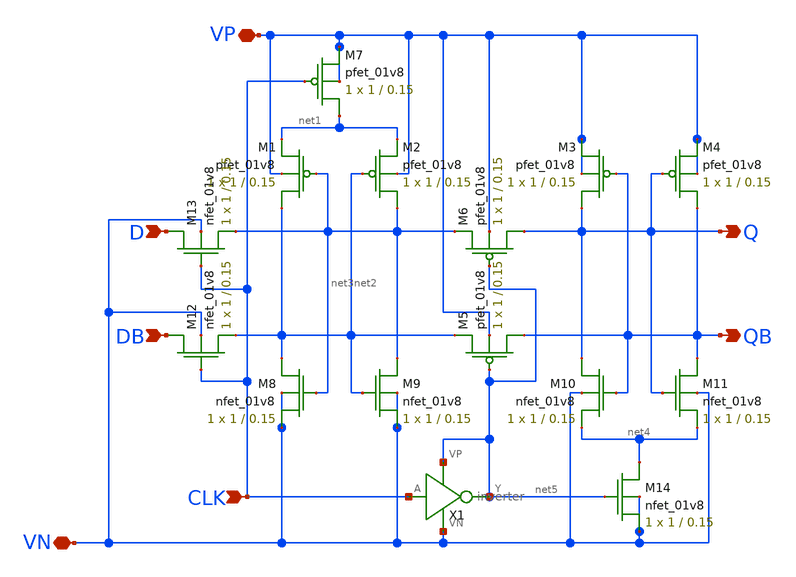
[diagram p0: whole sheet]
** sch_path: MP2/xschem/csrl_dff.sch
**.subckt csrl_dff D DB VP VN CLK QB Q
*.ipin D
*.ipin DB
*.iopin VP
*.iopin VN
*.ipin CLK
*.opin QB
*.opin Q
XM1 net2 net3 net1 VP sky130_fd_pr__pfet_01v8 L=0.15 W=1 nf=1 ad='int((nf+1)/2) * W/nf * 0.29' as='int((nf+2)/2) * W/nf * 0.29'
+ pd='2*int((nf+1)/2) * (W/nf + 0.29)' ps='2*int((nf+2)/2) * (W/nf + 0.29)' nrd='0.29 / W' nrs='0.29 / W'
+ sa=0 sb=0 sd=0 mult=1 m=1
XM2 net3 net2 net1 VP sky130_fd_pr__pfet_01v8 L=0.15 W=1 nf=1 ad='int((nf+1)/2) * W/nf * 0.29' as='int((nf+2)/2) * W/nf * 0.29'
+ pd='2*int((nf+1)/2) * (W/nf + 0.29)' ps='2*int((nf+2)/2) * (W/nf + 0.29)' nrd='0.29 / W' nrs='0.29 / W'
+ sa=0 sb=0 sd=0 mult=1 m=1
XM3 Q QB VP VP sky130_fd_pr__pfet_01v8 L=0.15 W=1 nf=1 ad='int((nf+1)/2) * W/nf * 0.29' as='int((nf+2)/2) * W/nf * 0.29'
+ pd='2*int((nf+1)/2) * (W/nf + 0.29)' ps='2*int((nf+2)/2) * (W/nf + 0.29)' nrd='0.29 / W' nrs='0.29 / W'
+ sa=0 sb=0 sd=0 mult=1 m=1
XM4 QB Q VP VP sky130_fd_pr__pfet_01v8 L=0.15 W=1 nf=1 ad='int((nf+1)/2) * W/nf * 0.29' as='int((nf+2)/2) * W/nf * 0.29'
+ pd='2*int((nf+1)/2) * (W/nf + 0.29)' ps='2*int((nf+2)/2) * (W/nf + 0.29)' nrd='0.29 / W' nrs='0.29 / W'
+ sa=0 sb=0 sd=0 mult=1 m=1
XM8 net2 net3 VN VN sky130_fd_pr__nfet_01v8 L=0.15 W=1 nf=1 ad='int((nf+1)/2) * W/nf * 0.29' as='int((nf+2)/2) * W/nf * 0.29'
+ pd='2*int((nf+1)/2) * (W/nf + 0.29)' ps='2*int((nf+2)/2) * (W/nf + 0.29)' nrd='0.29 / W' nrs='0.29 / W'
+ sa=0 sb=0 sd=0 mult=1 m=1
XM7 net1 CLK VP VP sky130_fd_pr__pfet_01v8 L=0.15 W=1 nf=1 ad='int((nf+1)/2) * W/nf * 0.29' as='int((nf+2)/2) * W/nf * 0.29'
+ pd='2*int((nf+1)/2) * (W/nf + 0.29)' ps='2*int((nf+2)/2) * (W/nf + 0.29)' nrd='0.29 / W' nrs='0.29 / W'
+ sa=0 sb=0 sd=0 mult=1 m=1
XM9 net3 net2 VN VN sky130_fd_pr__nfet_01v8 L=0.15 W=1 nf=1 ad='int((nf+1)/2) * W/nf * 0.29' as='int((nf+2)/2) * W/nf * 0.29'
+ pd='2*int((nf+1)/2) * (W/nf + 0.29)' ps='2*int((nf+2)/2) * (W/nf + 0.29)' nrd='0.29 / W' nrs='0.29 / W'
+ sa=0 sb=0 sd=0 mult=1 m=1
XM10 Q QB net4 VN sky130_fd_pr__nfet_01v8 L=0.15 W=1 nf=1 ad='int((nf+1)/2) * W/nf * 0.29' as='int((nf+2)/2) * W/nf * 0.29'
+ pd='2*int((nf+1)/2) * (W/nf + 0.29)' ps='2*int((nf+2)/2) * (W/nf + 0.29)' nrd='0.29 / W' nrs='0.29 / W'
+ sa=0 sb=0 sd=0 mult=1 m=1
XM11 QB Q net4 VN sky130_fd_pr__nfet_01v8 L=0.15 W=1 nf=1 ad='int((nf+1)/2) * W/nf * 0.29' as='int((nf+2)/2) * W/nf * 0.29'
+ pd='2*int((nf+1)/2) * (W/nf + 0.29)' ps='2*int((nf+2)/2) * (W/nf + 0.29)' nrd='0.29 / W' nrs='0.29 / W'
+ sa=0 sb=0 sd=0 mult=1 m=1
XM12 DB CLK net2 VN sky130_fd_pr__nfet_01v8 L=0.15 W=1 nf=1 ad='int((nf+1)/2) * W/nf * 0.29' as='int((nf+2)/2) * W/nf * 0.29'
+ pd='2*int((nf+1)/2) * (W/nf + 0.29)' ps='2*int((nf+2)/2) * (W/nf + 0.29)' nrd='0.29 / W' nrs='0.29 / W'
+ sa=0 sb=0 sd=0 mult=1 m=1
XM13 D CLK net3 VN sky130_fd_pr__nfet_01v8 L=0.15 W=1 nf=1 ad='int((nf+1)/2) * W/nf * 0.29' as='int((nf+2)/2) * W/nf * 0.29'
+ pd='2*int((nf+1)/2) * (W/nf + 0.29)' ps='2*int((nf+2)/2) * (W/nf + 0.29)' nrd='0.29 / W' nrs='0.29 / W'
+ sa=0 sb=0 sd=0 mult=1 m=1
XM14 net4 net5 VN VN sky130_fd_pr__nfet_01v8 L=0.15 W=1 nf=1 ad='int((nf+1)/2) * W/nf * 0.29' as='int((nf+2)/2) * W/nf * 0.29'
+ pd='2*int((nf+1)/2) * (W/nf + 0.29)' ps='2*int((nf+2)/2) * (W/nf + 0.29)' nrd='0.29 / W' nrs='0.29 / W'
+ sa=0 sb=0 sd=0 mult=1 m=1
XM5 QB net5 net2 VP sky130_fd_pr__pfet_01v8 L=0.15 W=1 nf=1 ad='int((nf+1)/2) * W/nf * 0.29' as='int((nf+2)/2) * W/nf * 0.29'
+ pd='2*int((nf+1)/2) * (W/nf + 0.29)' ps='2*int((nf+2)/2) * (W/nf + 0.29)' nrd='0.29 / W' nrs='0.29 / W'
+ sa=0 sb=0 sd=0 mult=1 m=1
XM6 Q net5 net3 VP sky130_fd_pr__pfet_01v8 L=0.15 W=1 nf=1 ad='int((nf+1)/2) * W/nf * 0.29' as='int((nf+2)/2) * W/nf * 0.29'
+ pd='2*int((nf+1)/2) * (W/nf + 0.29)' ps='2*int((nf+2)/2) * (W/nf + 0.29)' nrd='0.29 / W' nrs='0.29 / W'
+ sa=0 sb=0 sd=0 mult=1 m=1
X1 CLK net5 net5 VN inverter
**.ends
.end
